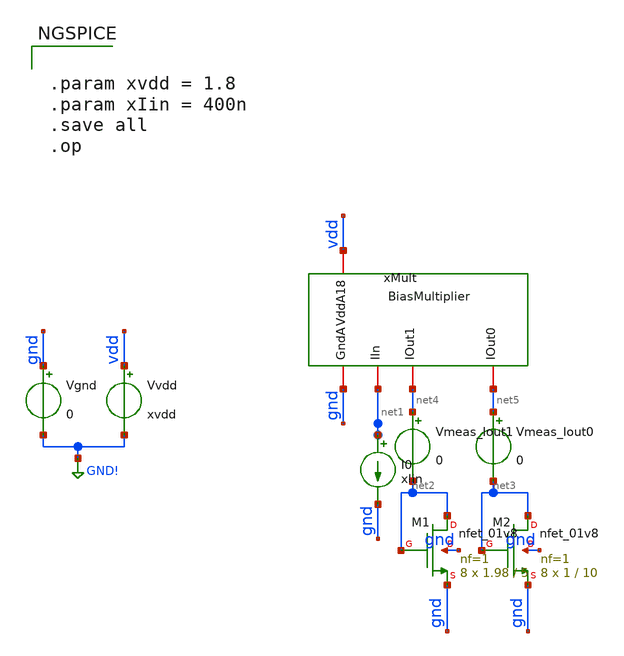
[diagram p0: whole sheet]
** sch_path: analog/xschem/tb_BiasMultiplier.sch
**.subckt tb_BiasMultiplier
Vgnd gnd GND! 0
.save i(vgnd)
Vvdd vdd GND! xvdd
.save i(vvdd)
I0 net1 gnd xIin
xMult gnd vdd net1 net4 net5 BiasMultiplier
XM1 net2 net2 gnd gnd sky130_fd_pr__nfet_01v8 L=5 W=1.98 nf=1 ad='int((1 + 1)/2) * 1.98 / 1 * 0.29' as='int((1 + 2)/2) * 1.98 / 1 * 0.29'
+ pd='2*int((1 + 1)/2) * (1.98 / 1 + 0.29)' ps='2*int((1 + 2)/2) * (1.98 / 1 + 0.29)' nrd='0.29 / 1.98 '
+ nrs='0.29 / 1.98 ' sa=0 sb=0 sd=0 mult=8 m=8
XM2 net3 net3 gnd gnd sky130_fd_pr__nfet_01v8 L=10 W=1 nf=1 ad='int((1 + 1)/2) * 1 / 1 * 0.29' as='int((1 + 2)/2) * 1 / 1 * 0.29'
+ pd='2*int((1 + 1)/2) * (1 / 1 + 0.29)' ps='2*int((1 + 2)/2) * (1 / 1 + 0.29)' nrd='0.29 / 1 ' nrs='0.29 / 1 '
+ sa=0 sb=0 sd=0 mult=8 m=8
Vmeas_Iout1 net4 net2 0
.save i(vmeas_iout1)
Vmeas_Iout0 net5 net3 0
.save i(vmeas_iout0)
**** begin user architecture code

** opencircuitdesign pdks install
.lib $::SKYWATER_MODELS/sky130.lib.spice tt



.param xvdd = 1.8
.param xIin = 400n
.save all
.op


**** end user architecture code
**.ends
.GLOBAL GND!
.end
